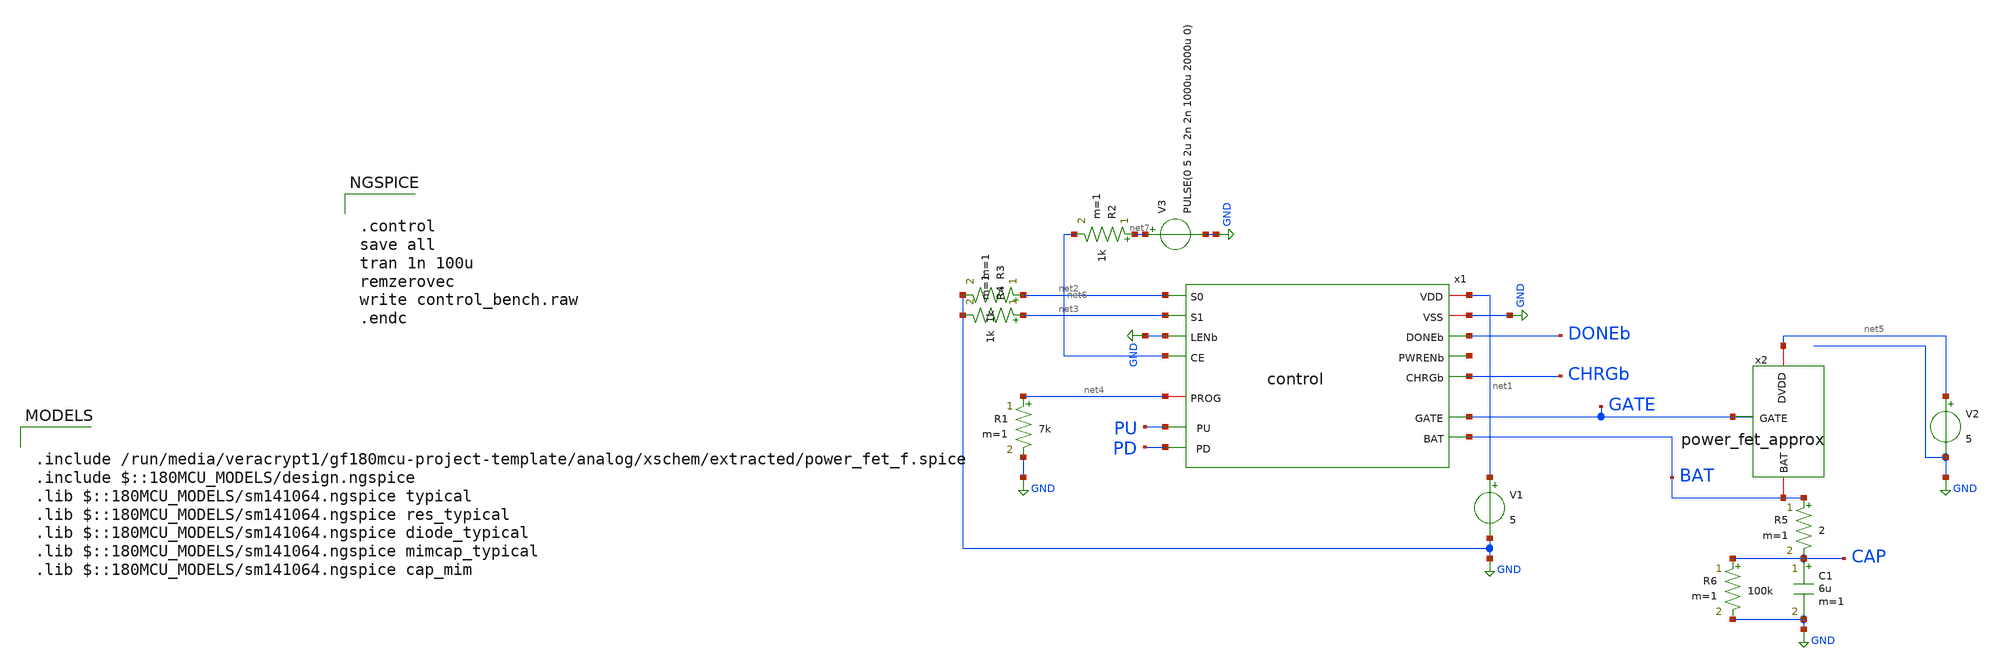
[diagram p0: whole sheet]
** sch_path: analog/xschem/control_bench.sch
**.subckt control_bench
x1 net1 GND net2 DONEb net3 GND net8 net6 BAT CHRGb net4 GATE PU PD control
V1 net1 GND 5
R1 net4 GND 7k m=1
R2 net7 net6 1k m=1
V2 net5 GND 5
R3 net2 GND 1k m=1
R4 net3 GND 1k m=1
V3 net7 GND PULSE(0 5 2u 2n 2n 1000u 2000u 0)
C1 CAP GND 6u m=1
R5 BAT CAP 2 m=1
R6 CAP GND 100k m=1
x2 net5 GATE BAT power_fet_approx
**** begin user architecture code


.control
save all
tran 1n 100u
remzerovec
write control_bench.raw
.endc



.include /run/media/veracrypt1/gf180mcu-project-template/analog/xschem/extracted/power_fet_f.spice
.include $::180MCU_MODELS/design.ngspice
.lib $::180MCU_MODELS/sm141064.ngspice typical
.lib $::180MCU_MODELS/sm141064.ngspice res_typical
.lib $::180MCU_MODELS/sm141064.ngspice diode_typical
.lib $::180MCU_MODELS/sm141064.ngspice mimcap_typical
.lib $::180MCU_MODELS/sm141064.ngspice cap_mim

**** end user architecture code
**.ends
.GLOBAL GND
.end
